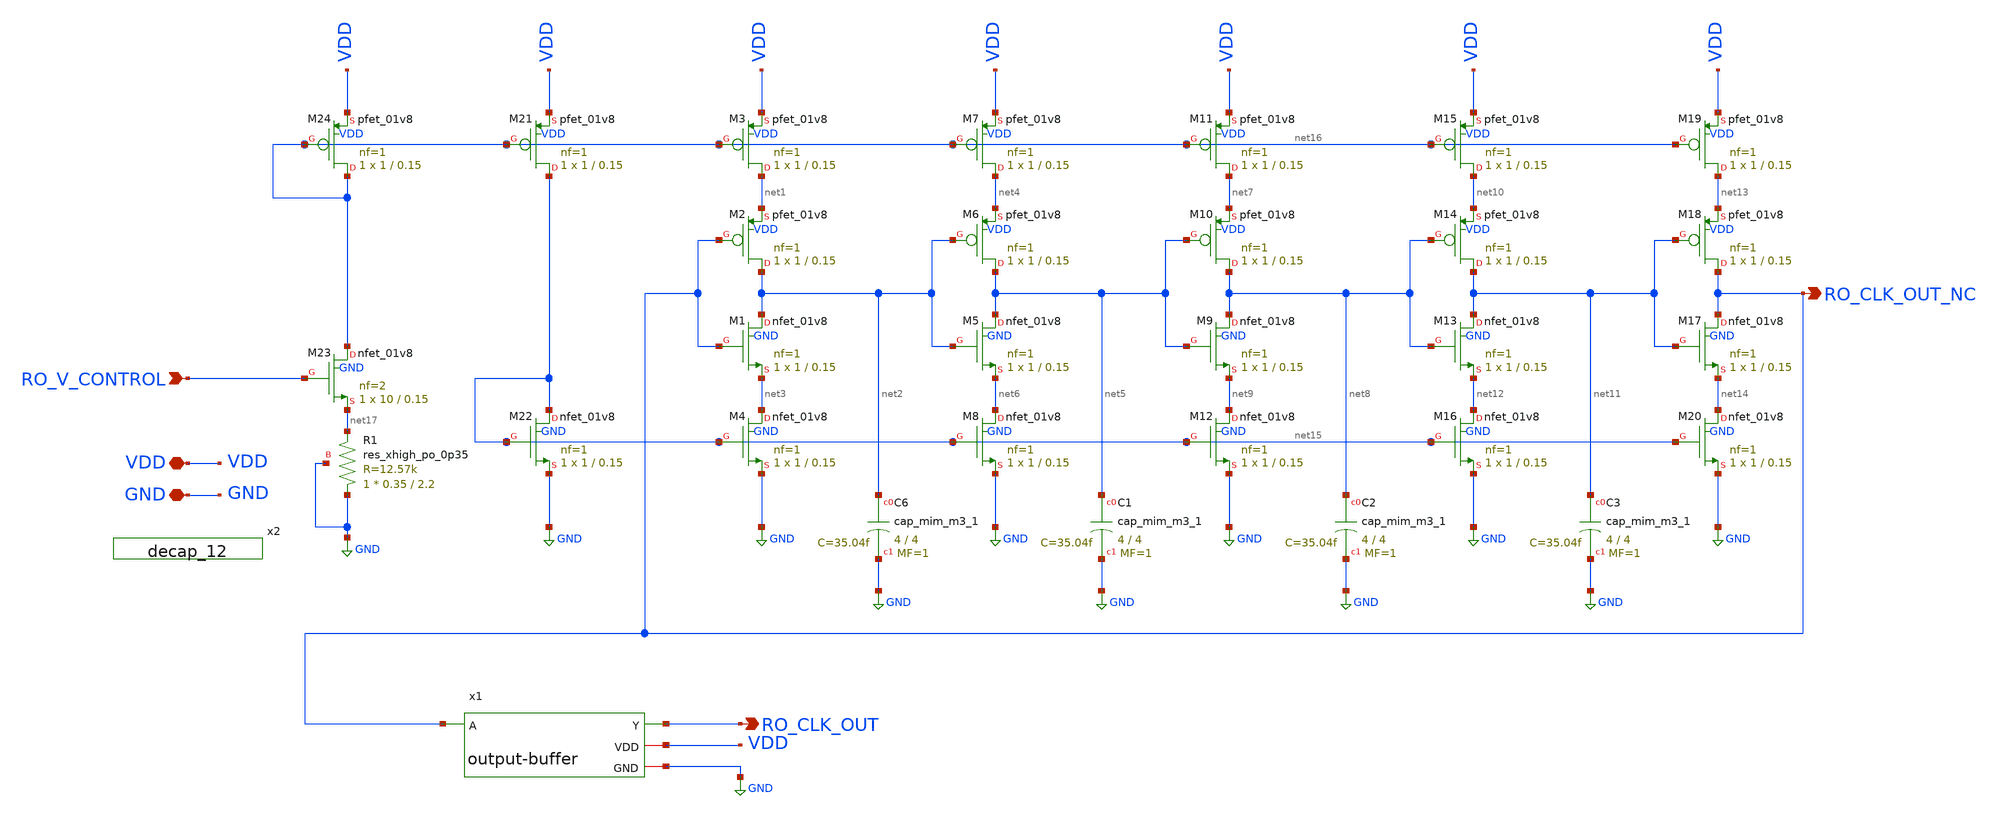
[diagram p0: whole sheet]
** sch_path: src/analog_source_files/RO-current-starved.sch
**.subckt RO-current-starved RO_V_CONTROL RO_CLK_OUT VDD GND RO_CLK_OUT_NC
*.ipin RO_V_CONTROL
*.opin RO_CLK_OUT
*.iopin VDD
*.iopin GND
*.opin RO_CLK_OUT_NC
XM1 net2 RO_CLK_OUT_NC net3 GND sky130_fd_pr__nfet_01v8 L=0.15 W=1 nf=1 ad='int((1 + 1)/2) * 1 / 1 * 0.29'
+ as='int((1 + 2)/2) * 1 / 1 * 0.29' pd='2*int((1 + 1)/2) * (1 / 1 + 0.29)' ps='2*int((1 + 2)/2) * (1 / 1 + 0.29)'
+ nrd='0.29 / 1 ' nrs='0.29 / 1 ' sa=0 sb=0 sd=0 mult=1 m=1
XM2 net2 RO_CLK_OUT_NC net1 VDD sky130_fd_pr__pfet_01v8 L=0.15 W=1 nf=1 ad='int((1 + 1)/2) * 1 / 1 * 0.29'
+ as='int((1 + 2)/2) * 1 / 1 * 0.29' pd='2*int((1 + 1)/2) * (1 / 1 + 0.29)' ps='2*int((1 + 2)/2) * (1 / 1 + 0.29)'
+ nrd='0.29 / 1 ' nrs='0.29 / 1 ' sa=0 sb=0 sd=0 mult=1 m=1
XM3 net1 net16 VDD VDD sky130_fd_pr__pfet_01v8 L=0.15 W=1 nf=1 ad='int((1 + 1)/2) * 1 / 1 * 0.29' as='int((1 + 2)/2) * 1 / 1 * 0.29'
+ pd='2*int((1 + 1)/2) * (1 / 1 + 0.29)' ps='2*int((1 + 2)/2) * (1 / 1 + 0.29)' nrd='0.29 / 1 ' nrs='0.29 / 1 '
+ sa=0 sb=0 sd=0 mult=1 m=1
XM4 net3 net15 GND GND sky130_fd_pr__nfet_01v8 L=0.15 W=1 nf=1 ad='int((1 + 1)/2) * 1 / 1 * 0.29' as='int((1 + 2)/2) * 1 / 1 * 0.29'
+ pd='2*int((1 + 1)/2) * (1 / 1 + 0.29)' ps='2*int((1 + 2)/2) * (1 / 1 + 0.29)' nrd='0.29 / 1 ' nrs='0.29 / 1 '
+ sa=0 sb=0 sd=0 mult=1 m=1
XM5 net5 net2 net6 GND sky130_fd_pr__nfet_01v8 L=0.15 W=1 nf=1 ad='int((1 + 1)/2) * 1 / 1 * 0.29' as='int((1 + 2)/2) * 1 / 1 * 0.29'
+ pd='2*int((1 + 1)/2) * (1 / 1 + 0.29)' ps='2*int((1 + 2)/2) * (1 / 1 + 0.29)' nrd='0.29 / 1 ' nrs='0.29 / 1 '
+ sa=0 sb=0 sd=0 mult=1 m=1
XM6 net5 net2 net4 VDD sky130_fd_pr__pfet_01v8 L=0.15 W=1 nf=1 ad='int((1 + 1)/2) * 1 / 1 * 0.29' as='int((1 + 2)/2) * 1 / 1 * 0.29'
+ pd='2*int((1 + 1)/2) * (1 / 1 + 0.29)' ps='2*int((1 + 2)/2) * (1 / 1 + 0.29)' nrd='0.29 / 1 ' nrs='0.29 / 1 '
+ sa=0 sb=0 sd=0 mult=1 m=1
XM7 net4 net16 VDD VDD sky130_fd_pr__pfet_01v8 L=0.15 W=1 nf=1 ad='int((1 + 1)/2) * 1 / 1 * 0.29' as='int((1 + 2)/2) * 1 / 1 * 0.29'
+ pd='2*int((1 + 1)/2) * (1 / 1 + 0.29)' ps='2*int((1 + 2)/2) * (1 / 1 + 0.29)' nrd='0.29 / 1 ' nrs='0.29 / 1 '
+ sa=0 sb=0 sd=0 mult=1 m=1
XM8 net6 net15 GND GND sky130_fd_pr__nfet_01v8 L=0.15 W=1 nf=1 ad='int((1 + 1)/2) * 1 / 1 * 0.29' as='int((1 + 2)/2) * 1 / 1 * 0.29'
+ pd='2*int((1 + 1)/2) * (1 / 1 + 0.29)' ps='2*int((1 + 2)/2) * (1 / 1 + 0.29)' nrd='0.29 / 1 ' nrs='0.29 / 1 '
+ sa=0 sb=0 sd=0 mult=1 m=1
XM9 net8 net5 net9 GND sky130_fd_pr__nfet_01v8 L=0.15 W=1 nf=1 ad='int((1 + 1)/2) * 1 / 1 * 0.29' as='int((1 + 2)/2) * 1 / 1 * 0.29'
+ pd='2*int((1 + 1)/2) * (1 / 1 + 0.29)' ps='2*int((1 + 2)/2) * (1 / 1 + 0.29)' nrd='0.29 / 1 ' nrs='0.29 / 1 '
+ sa=0 sb=0 sd=0 mult=1 m=1
XM10 net8 net5 net7 VDD sky130_fd_pr__pfet_01v8 L=0.15 W=1 nf=1 ad='int((1 + 1)/2) * 1 / 1 * 0.29' as='int((1 + 2)/2) * 1 / 1 * 0.29'
+ pd='2*int((1 + 1)/2) * (1 / 1 + 0.29)' ps='2*int((1 + 2)/2) * (1 / 1 + 0.29)' nrd='0.29 / 1 ' nrs='0.29 / 1 '
+ sa=0 sb=0 sd=0 mult=1 m=1
XM11 net7 net16 VDD VDD sky130_fd_pr__pfet_01v8 L=0.15 W=1 nf=1 ad='int((1 + 1)/2) * 1 / 1 * 0.29' as='int((1 + 2)/2) * 1 / 1 * 0.29'
+ pd='2*int((1 + 1)/2) * (1 / 1 + 0.29)' ps='2*int((1 + 2)/2) * (1 / 1 + 0.29)' nrd='0.29 / 1 ' nrs='0.29 / 1 '
+ sa=0 sb=0 sd=0 mult=1 m=1
XM12 net9 net15 GND GND sky130_fd_pr__nfet_01v8 L=0.15 W=1 nf=1 ad='int((1 + 1)/2) * 1 / 1 * 0.29' as='int((1 + 2)/2) * 1 / 1 * 0.29'
+ pd='2*int((1 + 1)/2) * (1 / 1 + 0.29)' ps='2*int((1 + 2)/2) * (1 / 1 + 0.29)' nrd='0.29 / 1 ' nrs='0.29 / 1 '
+ sa=0 sb=0 sd=0 mult=1 m=1
XM13 net11 net8 net12 GND sky130_fd_pr__nfet_01v8 L=0.15 W=1 nf=1 ad='int((1 + 1)/2) * 1 / 1 * 0.29'
+ as='int((1 + 2)/2) * 1 / 1 * 0.29' pd='2*int((1 + 1)/2) * (1 / 1 + 0.29)' ps='2*int((1 + 2)/2) * (1 / 1 + 0.29)'
+ nrd='0.29 / 1 ' nrs='0.29 / 1 ' sa=0 sb=0 sd=0 mult=1 m=1
XM14 net11 net8 net10 VDD sky130_fd_pr__pfet_01v8 L=0.15 W=1 nf=1 ad='int((1 + 1)/2) * 1 / 1 * 0.29'
+ as='int((1 + 2)/2) * 1 / 1 * 0.29' pd='2*int((1 + 1)/2) * (1 / 1 + 0.29)' ps='2*int((1 + 2)/2) * (1 / 1 + 0.29)'
+ nrd='0.29 / 1 ' nrs='0.29 / 1 ' sa=0 sb=0 sd=0 mult=1 m=1
XM15 net10 net16 VDD VDD sky130_fd_pr__pfet_01v8 L=0.15 W=1 nf=1 ad='int((1 + 1)/2) * 1 / 1 * 0.29' as='int((1 + 2)/2) * 1 / 1 * 0.29'
+ pd='2*int((1 + 1)/2) * (1 / 1 + 0.29)' ps='2*int((1 + 2)/2) * (1 / 1 + 0.29)' nrd='0.29 / 1 ' nrs='0.29 / 1 '
+ sa=0 sb=0 sd=0 mult=1 m=1
XM16 net12 net15 GND GND sky130_fd_pr__nfet_01v8 L=0.15 W=1 nf=1 ad='int((1 + 1)/2) * 1 / 1 * 0.29' as='int((1 + 2)/2) * 1 / 1 * 0.29'
+ pd='2*int((1 + 1)/2) * (1 / 1 + 0.29)' ps='2*int((1 + 2)/2) * (1 / 1 + 0.29)' nrd='0.29 / 1 ' nrs='0.29 / 1 '
+ sa=0 sb=0 sd=0 mult=1 m=1
XM17 RO_CLK_OUT_NC net11 net14 GND sky130_fd_pr__nfet_01v8 L=0.15 W=1 nf=1 ad='int((1 + 1)/2) * 1 / 1 * 0.29'
+ as='int((1 + 2)/2) * 1 / 1 * 0.29' pd='2*int((1 + 1)/2) * (1 / 1 + 0.29)' ps='2*int((1 + 2)/2) * (1 / 1 + 0.29)'
+ nrd='0.29 / 1 ' nrs='0.29 / 1 ' sa=0 sb=0 sd=0 mult=1 m=1
XM18 RO_CLK_OUT_NC net11 net13 VDD sky130_fd_pr__pfet_01v8 L=0.15 W=1 nf=1 ad='int((1 + 1)/2) * 1 / 1 * 0.29'
+ as='int((1 + 2)/2) * 1 / 1 * 0.29' pd='2*int((1 + 1)/2) * (1 / 1 + 0.29)' ps='2*int((1 + 2)/2) * (1 / 1 + 0.29)'
+ nrd='0.29 / 1 ' nrs='0.29 / 1 ' sa=0 sb=0 sd=0 mult=1 m=1
XM19 net13 net16 VDD VDD sky130_fd_pr__pfet_01v8 L=0.15 W=1 nf=1 ad='int((1 + 1)/2) * 1 / 1 * 0.29' as='int((1 + 2)/2) * 1 / 1 * 0.29'
+ pd='2*int((1 + 1)/2) * (1 / 1 + 0.29)' ps='2*int((1 + 2)/2) * (1 / 1 + 0.29)' nrd='0.29 / 1 ' nrs='0.29 / 1 '
+ sa=0 sb=0 sd=0 mult=1 m=1
XM20 net14 net15 GND GND sky130_fd_pr__nfet_01v8 L=0.15 W=1 nf=1 ad='int((1 + 1)/2) * 1 / 1 * 0.29' as='int((1 + 2)/2) * 1 / 1 * 0.29'
+ pd='2*int((1 + 1)/2) * (1 / 1 + 0.29)' ps='2*int((1 + 2)/2) * (1 / 1 + 0.29)' nrd='0.29 / 1 ' nrs='0.29 / 1 '
+ sa=0 sb=0 sd=0 mult=1 m=1
XM21 net15 net16 VDD VDD sky130_fd_pr__pfet_01v8 L=0.15 W=1 nf=1 ad='int((1 + 1)/2) * 1 / 1 * 0.29' as='int((1 + 2)/2) * 1 / 1 * 0.29'
+ pd='2*int((1 + 1)/2) * (1 / 1 + 0.29)' ps='2*int((1 + 2)/2) * (1 / 1 + 0.29)' nrd='0.29 / 1 ' nrs='0.29 / 1 '
+ sa=0 sb=0 sd=0 mult=1 m=1
XM22 net15 net15 GND GND sky130_fd_pr__nfet_01v8 L=0.15 W=1 nf=1 ad='int((1 + 1)/2) * 1 / 1 * 0.29' as='int((1 + 2)/2) * 1 / 1 * 0.29'
+ pd='2*int((1 + 1)/2) * (1 / 1 + 0.29)' ps='2*int((1 + 2)/2) * (1 / 1 + 0.29)' nrd='0.29 / 1 ' nrs='0.29 / 1 '
+ sa=0 sb=0 sd=0 mult=1 m=1
XM23 net16 RO_V_CONTROL net17 GND sky130_fd_pr__nfet_01v8 L=0.15 W=10 nf=2 ad='int((2 + 1)/2) * 10 / 2 * 0.29'
+ as='int((2 + 2)/2) * 10 / 2 * 0.29' pd='2*int((2 + 1)/2) * (10 / 2 + 0.29)' ps='2*int((2 + 2)/2) * (10 / 2 + 0.29)'
+ nrd='0.29 / 10 ' nrs='0.29 / 10 ' sa=0 sb=0 sd=0 mult=1 m=1
XM24 net16 net16 VDD VDD sky130_fd_pr__pfet_01v8 L=0.15 W=1 nf=1 ad='int((1 + 1)/2) * 1 / 1 * 0.29' as='int((1 + 2)/2) * 1 / 1 * 0.29'
+ pd='2*int((1 + 1)/2) * (1 / 1 + 0.29)' ps='2*int((1 + 2)/2) * (1 / 1 + 0.29)' nrd='0.29 / 1 ' nrs='0.29 / 1 '
+ sa=0 sb=0 sd=0 mult=1 m=1
x1 RO_CLK_OUT RO_CLK_OUT_NC VDD GND output-buffer
XC6 net2 GND sky130_fd_pr__cap_mim_m3_1 W=4 L=4 MF=1 m=1
XC1 net5 GND sky130_fd_pr__cap_mim_m3_1 W=4 L=4 MF=1 m=1
XC2 net8 GND sky130_fd_pr__cap_mim_m3_1 W=4 L=4 MF=1 m=1
XC3 net11 GND sky130_fd_pr__cap_mim_m3_1 W=4 L=4 MF=1 m=1
x2 GND GND VDD VDD sky130_fd_sc_hd__decap_12
XR1 GND net17 GND sky130_fd_pr__res_xhigh_po_0p35 L=2.2 mult=1 m=1
**.ends

* expanding   symbol:  output-buffer.sym # of pins=4
** sym_path: src/analog_source_files/output-buffer.sym
** sch_path: src/analog_source_files/output-buffer.sch
.subckt output-buffer Y A VDD GND
*.ipin A
*.opin Y
*.iopin VDD
*.iopin GND
XM31 net1 A GND GND sky130_fd_pr__nfet_01v8 L=0.15 W=0.7 nf=1 ad='int((1 + 1)/2) * 0.7 / 1 * 0.29' as='int((1 + 2)/2) * 0.7 / 1 * 0.29'
+ pd='2*int((1 + 1)/2) * (0.7 / 1 + 0.29)' ps='2*int((1 + 2)/2) * (0.7 / 1 + 0.29)' nrd='0.29 / 0.7 ' nrs='0.29 / 0.7 '
+ sa=0 sb=0 sd=0 mult=1 m=1
XM32 net1 A VDD VDD sky130_fd_pr__pfet_01v8 L=0.15 W=0.7 nf=1 ad='int((1 + 1)/2) * 0.7 / 1 * 0.29' as='int((1 + 2)/2) * 0.7 / 1 * 0.29'
+ pd='2*int((1 + 1)/2) * (0.7 / 1 + 0.29)' ps='2*int((1 + 2)/2) * (0.7 / 1 + 0.29)' nrd='0.29 / 0.7 ' nrs='0.29 / 0.7 '
+ sa=0 sb=0 sd=0 mult=1 m=1
XM33 net2 net1 GND GND sky130_fd_pr__nfet_01v8 L=0.15 W=2 nf=1 ad='int((1 + 1)/2) * 2 / 1 * 0.29' as='int((1 + 2)/2) * 2 / 1 * 0.29'
+ pd='2*int((1 + 1)/2) * (2 / 1 + 0.29)' ps='2*int((1 + 2)/2) * (2 / 1 + 0.29)' nrd='0.29 / 2 ' nrs='0.29 / 2 '
+ sa=0 sb=0 sd=0 mult=1 m=1
XM34 net2 net1 VDD VDD sky130_fd_pr__pfet_01v8 L=0.15 W=2 nf=1 ad='int((1 + 1)/2) * 2 / 1 * 0.29' as='int((1 + 2)/2) * 2 / 1 * 0.29'
+ pd='2*int((1 + 1)/2) * (2 / 1 + 0.29)' ps='2*int((1 + 2)/2) * (2 / 1 + 0.29)' nrd='0.29 / 2 ' nrs='0.29 / 2 '
+ sa=0 sb=0 sd=0 mult=1 m=1
XM35 net3 net2 GND GND sky130_fd_pr__nfet_01v8 L=0.15 W=4.5 nf=1 ad='int((1 + 1)/2) * 4.5 / 1 * 0.29'
+ as='int((1 + 2)/2) * 4.5 / 1 * 0.29' pd='2*int((1 + 1)/2) * (4.5 / 1 + 0.29)' ps='2*int((1 + 2)/2) * (4.5 / 1 + 0.29)'
+ nrd='0.29 / 4.5 ' nrs='0.29 / 4.5 ' sa=0 sb=0 sd=0 mult=1 m=1
XM36 net3 net2 VDD VDD sky130_fd_pr__pfet_01v8 L=0.15 W=4.5 nf=1 ad='int((1 + 1)/2) * 4.5 / 1 * 0.29'
+ as='int((1 + 2)/2) * 4.5 / 1 * 0.29' pd='2*int((1 + 1)/2) * (4.5 / 1 + 0.29)' ps='2*int((1 + 2)/2) * (4.5 / 1 + 0.29)'
+ nrd='0.29 / 4.5 ' nrs='0.29 / 4.5 ' sa=0 sb=0 sd=0 mult=1 m=1
XM25 Y net3 GND GND sky130_fd_pr__nfet_01v8 L=0.15 W=15 nf=3 ad='int((3 + 1)/2) * 15 / 3 * 0.29' as='int((3 + 2)/2) * 15 / 3 * 0.29'
+ pd='2*int((3 + 1)/2) * (15 / 3 + 0.29)' ps='2*int((3 + 2)/2) * (15 / 3 + 0.29)' nrd='0.29 / 15 ' nrs='0.29 / 15 '
+ sa=0 sb=0 sd=0 mult=1 m=1
XM26 Y net3 VDD VDD sky130_fd_pr__pfet_01v8 L=0.15 W=7 nf=3 ad='int((3 + 1)/2) * 7 / 3 * 0.29' as='int((3 + 2)/2) * 7 / 3 * 0.29'
+ pd='2*int((3 + 1)/2) * (7 / 3 + 0.29)' ps='2*int((3 + 2)/2) * (7 / 3 + 0.29)' nrd='0.29 / 7 ' nrs='0.29 / 7 '
+ sa=0 sb=0 sd=0 mult=1 m=1
x1 GND GND VDD VDD sky130_fd_sc_hd__decap_12
x2 GND GND VDD VDD sky130_fd_sc_hd__decap_12
**** begin user architecture code


.include /foss/pdks/sky130A/libs.ref/sky130_fd_sc_hd/spice/sky130_fd_sc_hd.spice


**** end user architecture code
.ends

.GLOBAL GND
.end
